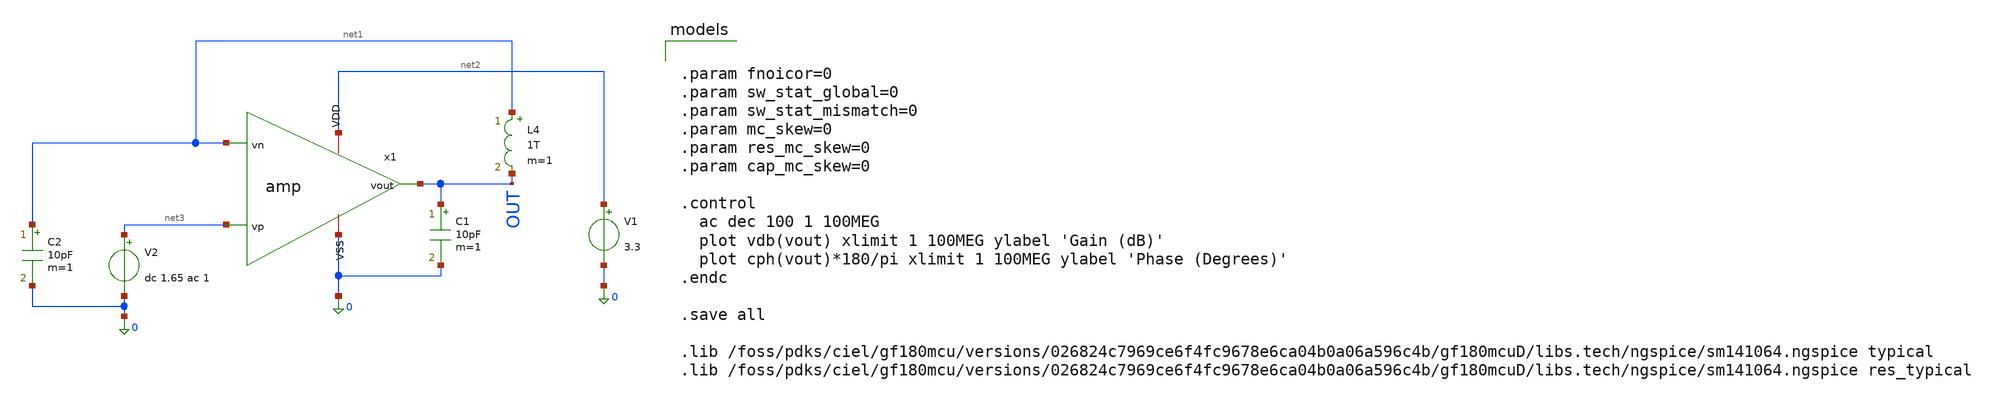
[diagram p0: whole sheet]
** sch_path: xschem/amp_tb_ac.sch
**.subckt amp_tb_ac
x1 net2 OUT net1 net3 0 amp
V1 net2 0 3.3
V2 net3 0 dc 1.65 ac 1
C1 OUT 0 10pF m=1
L4 net1 OUT 1T m=1
C2 net1 0 10pF m=1
**** begin user architecture code


.param fnoicor=0
.param sw_stat_global=0
.param sw_stat_mismatch=0
.param mc_skew=0
.param res_mc_skew=0
.param cap_mc_skew=0

.control
  ac dec 100 1 100MEG
  plot vdb(vout) xlimit 1 100MEG ylabel 'Gain (dB)'
  plot cph(vout)*180/pi xlimit 1 100MEG ylabel 'Phase (Degrees)'
.endc

.save all

.lib /foss/pdks/ciel/gf180mcu/versions/026824c7969ce6f4fc9678e6ca04b0a06a596c4b/gf180mcuD/libs.tech/ngspice/sm141064.ngspice typical
.lib /foss/pdks/ciel/gf180mcu/versions/026824c7969ce6f4fc9678e6ca04b0a06a596c4b/gf180mcuD/libs.tech/ngspice/sm141064.ngspice res_typical


**** end user architecture code
**.ends

* expanding   symbol:  xschem/amp.sym # of pins=5
** sym_path: xschem/amp.sym
** sch_path: xschem/amp.sch
.subckt amp VDD vout vn vp VSS
*.iopin VDD
*.iopin VSS
*.ipin vn
*.ipin vp
*.opin vout
XM1 net1 net1 VDD VDD pfet_03v3 L=0.5u W=8u nf=1 ad='int((nf+1)/2) * W/nf * 0.18u' as='int((nf+2)/2) * W/nf * 0.18u'
+ pd='2*int((nf+1)/2) * (W/nf + 0.18u)' ps='2*int((nf+2)/2) * (W/nf + 0.18u)' nrd='0.18u / W' nrs='0.18u / W'
+ sa=0 sb=0 sd=0 m=1 par=1
XM2 net3 net1 VDD VDD pfet_03v3 L=0.5u W=8u nf=1 ad='int((nf+1)/2) * W/nf * 0.18u' as='int((nf+2)/2) * W/nf * 0.18u'
+ pd='2*int((nf+1)/2) * (W/nf + 0.18u)' ps='2*int((nf+2)/2) * (W/nf + 0.18u)' nrd='0.18u / W' nrs='0.18u / W'
+ sa=0 sb=0 sd=0 m=1 par=1
XM3 net4 vp net3 VDD pfet_03v3 L=0.5u W=4u nf=1 ad='int((nf+1)/2) * W/nf * 0.18u' as='int((nf+2)/2) * W/nf * 0.18u'
+ pd='2*int((nf+1)/2) * (W/nf + 0.18u)' ps='2*int((nf+2)/2) * (W/nf + 0.18u)' nrd='0.18u / W' nrs='0.18u / W'
+ sa=0 sb=0 sd=0 m=1 par=1
XM4 net2 vn net3 VDD pfet_03v3 L=0.5u W=4u nf=1 ad='int((nf+1)/2) * W/nf * 0.18u' as='int((nf+2)/2) * W/nf * 0.18u'
+ pd='2*int((nf+1)/2) * (W/nf + 0.18u)' ps='2*int((nf+2)/2) * (W/nf + 0.18u)' nrd='0.18u / W' nrs='0.18u / W'
+ sa=0 sb=0 sd=0 m=1 par=1
XM5 vout net1 VDD VDD pfet_03v3 L=0.5u W=20u nf=1 ad='int((nf+1)/2) * W/nf * 0.18u' as='int((nf+2)/2) * W/nf * 0.18u'
+ pd='2*int((nf+1)/2) * (W/nf + 0.18u)' ps='2*int((nf+2)/2) * (W/nf + 0.18u)' nrd='0.18u / W' nrs='0.18u / W'
+ sa=0 sb=0 sd=0 m=1 par=1
XM6 net4 net2 VSS VSS nfet_03v3 L=0.5u W=1u nf=1 ad='int((nf+1)/2) * W/nf * 0.18u' as='int((nf+2)/2) * W/nf * 0.18u'
+ pd='2*int((nf+1)/2) * (W/nf + 0.18u)' ps='2*int((nf+2)/2) * (W/nf + 0.18u)' nrd='0.18u / W' nrs='0.18u / W'
+ sa=0 sb=0 sd=0 m=1 par=1
XM8 vout net4 VSS VSS nfet_03v3 L=0.5u W=5u nf=1 ad='int((nf+1)/2) * W/nf * 0.18u' as='int((nf+2)/2) * W/nf * 0.18u'
+ pd='2*int((nf+1)/2) * (W/nf + 0.18u)' ps='2*int((nf+2)/2) * (W/nf + 0.18u)' nrd='0.18u / W' nrs='0.18u / W'
+ sa=0 sb=0 sd=0 m=1 par=1
XR1 VSS net1 VSS ppolyf_u_1k r_width=1u r_length=120u m=1
C1 vout net4 2.5p m=1
XM7 net2 net2 VSS VSS nfet_03v3 L=0.5u W=1u nf=1 ad='int((nf+1)/2) * W/nf * 0.18u' as='int((nf+2)/2) * W/nf * 0.18u'
+ pd='2*int((nf+1)/2) * (W/nf + 0.18u)' ps='2*int((nf+2)/2) * (W/nf + 0.18u)' nrd='0.18u / W' nrs='0.18u / W'
+ sa=0 sb=0 sd=0 m=1 par=1
.ends

.end
